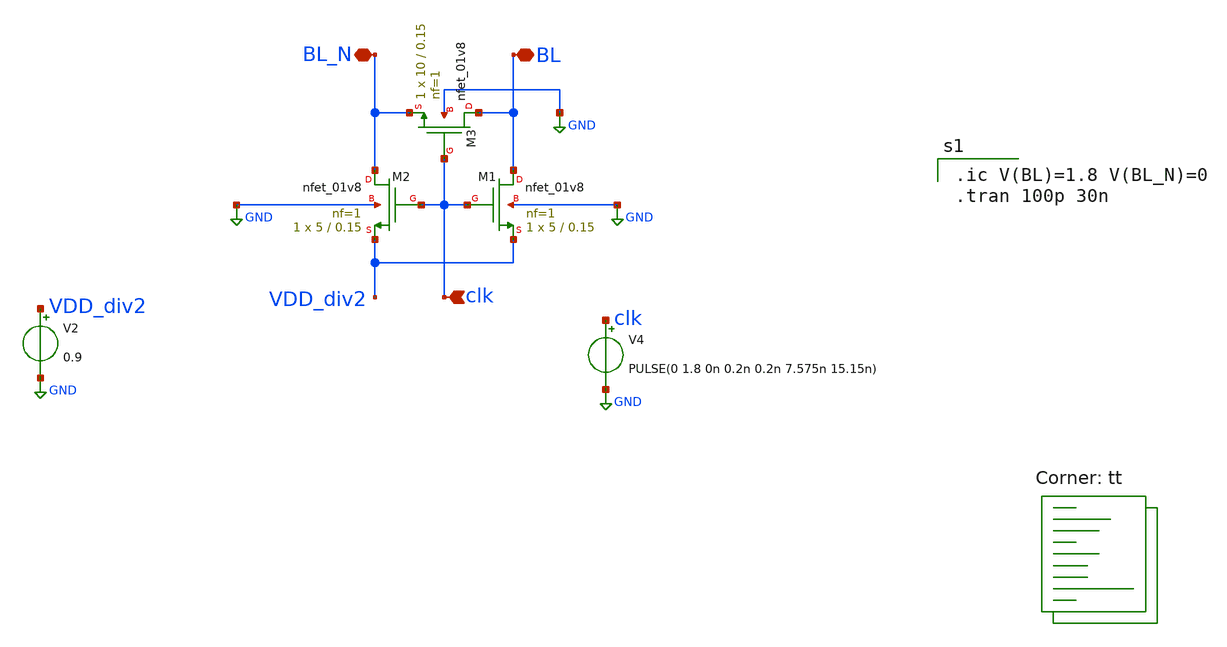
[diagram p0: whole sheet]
** sch_path: analog/schematics/power.sch
**.subckt power BL BL_N clk
*.iopin BL
*.iopin BL_N
*.ipin clk
XM1 BL clk VDD_div2 GND sky130_fd_pr__nfet_01v8 L=0.15 W=5 nf=1 ad='int((nf+1)/2) * W/nf * 0.29' as='int((nf+2)/2) * W/nf * 0.29'
+ pd='2*int((nf+1)/2) * (W/nf + 0.29)' ps='2*int((nf+2)/2) * (W/nf + 0.29)' nrd='0.29 / W' nrs='0.29 / W'
+ sa=0 sb=0 sd=0 mult=1 m=1
XM2 BL_N clk VDD_div2 GND sky130_fd_pr__nfet_01v8 L=0.15 W=5 nf=1 ad='int((nf+1)/2) * W/nf * 0.29' as='int((nf+2)/2) * W/nf * 0.29'
+ pd='2*int((nf+1)/2) * (W/nf + 0.29)' ps='2*int((nf+2)/2) * (W/nf + 0.29)' nrd='0.29 / W' nrs='0.29 / W'
+ sa=0 sb=0 sd=0 mult=1 m=1
XM3 BL clk BL_N GND sky130_fd_pr__nfet_01v8 L=0.15 W=10 nf=1 ad='int((nf+1)/2) * W/nf * 0.29' as='int((nf+2)/2) * W/nf * 0.29'
+ pd='2*int((nf+1)/2) * (W/nf + 0.29)' ps='2*int((nf+2)/2) * (W/nf + 0.29)' nrd='0.29 / W' nrs='0.29 / W'
+ sa=0 sb=0 sd=0 mult=1 m=1
V2 VDD_div2 GND 0.9
V4 clk GND PULSE(0 1.8 0n 0.2n 0.2n 7.575n 15.15n)
**** begin user architecture code

.ic V(BL)=1.8 V(BL_N)=0
.tran 100p 30n

.lib $::SKYWATER_MODELS/sky130.lib.spice tt
**** end user architecture code
**.ends
.GLOBAL GND
.end
